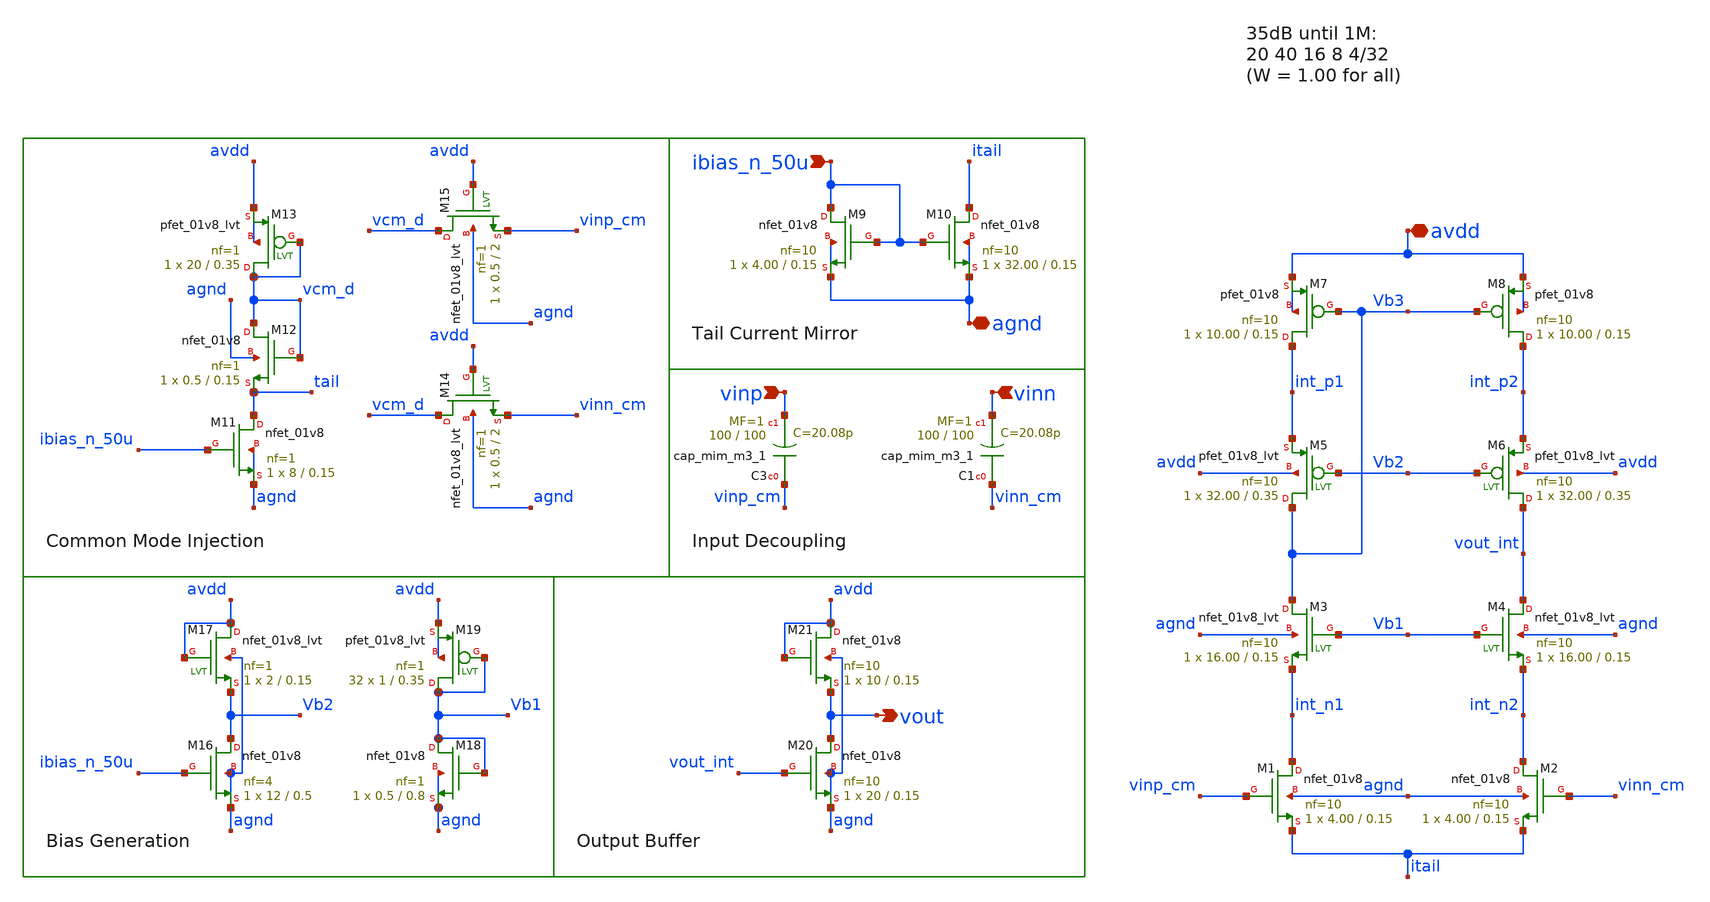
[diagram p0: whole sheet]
** sch_path: AMP/Final_Cascode_Mixed.sch
**.subckt Final_Cascode_Mixed avdd vinp vout agnd vinn ibias_n_50u
*.iopin avdd
*.ipin vinp
*.opin vout
*.iopin agnd
*.ipin vinn
*.ipin ibias_n_50u
XM1 int_n1 vinp_cm itail agnd sky130_fd_pr__nfet_01v8 L=0.15 W=4.00 nf=10 ad='int((nf+1)/2) * W/nf * 0.29'
+ as='int((nf+2)/2) * W/nf * 0.29' pd='2*int((nf+1)/2) * (W/nf + 0.29)' ps='2*int((nf+2)/2) * (W/nf + 0.29)'
+ nrd='0.29 / W' nrs='0.29 / W' sa=0 sb=0 sd=0 mult=1 m=1
XM2 int_n2 vinn_cm itail agnd sky130_fd_pr__nfet_01v8 L=0.15 W=4.00 nf=10 ad='int((nf+1)/2) * W/nf * 0.29'
+ as='int((nf+2)/2) * W/nf * 0.29' pd='2*int((nf+1)/2) * (W/nf + 0.29)' ps='2*int((nf+2)/2) * (W/nf + 0.29)'
+ nrd='0.29 / W' nrs='0.29 / W' sa=0 sb=0 sd=0 mult=1 m=1
XM7 int_p1 Vb3 avdd avdd sky130_fd_pr__pfet_01v8 L=0.15 W=10.00 nf=10 ad='int((nf+1)/2) * W/nf * 0.29'
+ as='int((nf+2)/2) * W/nf * 0.29' pd='2*int((nf+1)/2) * (W/nf + 0.29)' ps='2*int((nf+2)/2) * (W/nf + 0.29)'
+ nrd='0.29 / W' nrs='0.29 / W' sa=0 sb=0 sd=0 mult=1 m=1
XM8 int_p2 Vb3 avdd avdd sky130_fd_pr__pfet_01v8 L=0.15 W=10.00 nf=10 ad='int((nf+1)/2) * W/nf * 0.29'
+ as='int((nf+2)/2) * W/nf * 0.29' pd='2*int((nf+1)/2) * (W/nf + 0.29)' ps='2*int((nf+2)/2) * (W/nf + 0.29)'
+ nrd='0.29 / W' nrs='0.29 / W' sa=0 sb=0 sd=0 mult=1 m=1
XM9 ibias_n_50u ibias_n_50u agnd agnd sky130_fd_pr__nfet_01v8 L=0.15 W=4.00 nf=10 ad='int((nf+1)/2) * W/nf * 0.29'
+ as='int((nf+2)/2) * W/nf * 0.29' pd='2*int((nf+1)/2) * (W/nf + 0.29)' ps='2*int((nf+2)/2) * (W/nf + 0.29)'
+ nrd='0.29 / W' nrs='0.29 / W' sa=0 sb=0 sd=0 mult=1 m=1
XM10 itail ibias_n_50u agnd agnd sky130_fd_pr__nfet_01v8 L=0.15 W=32.00 nf=10 ad='int((nf+1)/2) * W/nf * 0.29'
+ as='int((nf+2)/2) * W/nf * 0.29' pd='2*int((nf+1)/2) * (W/nf + 0.29)' ps='2*int((nf+2)/2) * (W/nf + 0.29)'
+ nrd='0.29 / W' nrs='0.29 / W' sa=0 sb=0 sd=0 mult=1 m=1
XM3 Vb3 Vb1 int_n1 agnd sky130_fd_pr__nfet_01v8_lvt L=0.15 W=16.00 nf=10 ad='int((nf+1)/2) * W/nf * 0.29'
+ as='int((nf+2)/2) * W/nf * 0.29' pd='2*int((nf+1)/2) * (W/nf + 0.29)' ps='2*int((nf+2)/2) * (W/nf + 0.29)'
+ nrd='0.29 / W' nrs='0.29 / W' sa=0 sb=0 sd=0 mult=1 m=1
XM4 vout_int Vb1 int_n2 agnd sky130_fd_pr__nfet_01v8_lvt L=0.15 W=16.00 nf=10 ad='int((nf+1)/2) * W/nf * 0.29'
+ as='int((nf+2)/2) * W/nf * 0.29' pd='2*int((nf+1)/2) * (W/nf + 0.29)' ps='2*int((nf+2)/2) * (W/nf + 0.29)'
+ nrd='0.29 / W' nrs='0.29 / W' sa=0 sb=0 sd=0 mult=1 m=1
XM5 Vb3 Vb2 int_p1 avdd sky130_fd_pr__pfet_01v8_lvt L=0.35 W=32.00 nf=10 ad='int((nf+1)/2) * W/nf * 0.29'
+ as='int((nf+2)/2) * W/nf * 0.29' pd='2*int((nf+1)/2) * (W/nf + 0.29)' ps='2*int((nf+2)/2) * (W/nf + 0.29)'
+ nrd='0.29 / W' nrs='0.29 / W' sa=0 sb=0 sd=0 mult=1 m=1
XM6 vout_int Vb2 int_p2 avdd sky130_fd_pr__pfet_01v8_lvt L=0.35 W=32.00 nf=10 ad='int((nf+1)/2) * W/nf * 0.29'
+ as='int((nf+2)/2) * W/nf * 0.29' pd='2*int((nf+1)/2) * (W/nf + 0.29)' ps='2*int((nf+2)/2) * (W/nf + 0.29)'
+ nrd='0.29 / W' nrs='0.29 / W' sa=0 sb=0 sd=0 mult=1 m=1
XM11 tail ibias_n_50u agnd agnd sky130_fd_pr__nfet_01v8 L=0.15 W=8 nf=1 ad='int((nf+1)/2) * W/nf * 0.29'
+ as='int((nf+2)/2) * W/nf * 0.29' pd='2*int((nf+1)/2) * (W/nf + 0.29)' ps='2*int((nf+2)/2) * (W/nf + 0.29)'
+ nrd='0.29 / W' nrs='0.29 / W' sa=0 sb=0 sd=0 mult=1 m=1
XM12 vcm_d vcm_d tail agnd sky130_fd_pr__nfet_01v8 L=0.15 W=0.5 nf=1 ad='int((nf+1)/2) * W/nf * 0.29'
+ as='int((nf+2)/2) * W/nf * 0.29' pd='2*int((nf+1)/2) * (W/nf + 0.29)' ps='2*int((nf+2)/2) * (W/nf + 0.29)'
+ nrd='0.29 / W' nrs='0.29 / W' sa=0 sb=0 sd=0 mult=1 m=1
XM13 vcm_d vcm_d avdd avdd sky130_fd_pr__pfet_01v8_lvt L=0.35 W=20 nf=1 ad='int((nf+1)/2) * W/nf * 0.29'
+ as='int((nf+2)/2) * W/nf * 0.29' pd='2*int((nf+1)/2) * (W/nf + 0.29)' ps='2*int((nf+2)/2) * (W/nf + 0.29)'
+ nrd='0.29 / W' nrs='0.29 / W' sa=0 sb=0 sd=0 mult=1 m=1
XM14 vcm_d avdd vinn_cm agnd sky130_fd_pr__nfet_01v8_lvt L=2 W=0.5 nf=1 ad='int((nf+1)/2) * W/nf * 0.29'
+ as='int((nf+2)/2) * W/nf * 0.29' pd='2*int((nf+1)/2) * (W/nf + 0.29)' ps='2*int((nf+2)/2) * (W/nf + 0.29)'
+ nrd='0.29 / W' nrs='0.29 / W' sa=0 sb=0 sd=0 mult=1 m=1
XM15 vcm_d avdd vinp_cm agnd sky130_fd_pr__nfet_01v8_lvt L=2 W=0.5 nf=1 ad='int((nf+1)/2) * W/nf * 0.29'
+ as='int((nf+2)/2) * W/nf * 0.29' pd='2*int((nf+1)/2) * (W/nf + 0.29)' ps='2*int((nf+2)/2) * (W/nf + 0.29)'
+ nrd='0.29 / W' nrs='0.29 / W' sa=0 sb=0 sd=0 mult=1 m=1
XC3 vinp_cm vinp sky130_fd_pr__cap_mim_m3_1 W=100 L=100 MF=1 m=1
XC1 vinn_cm vinn sky130_fd_pr__cap_mim_m3_1 W=100 L=100 MF=1 m=1
XM16 Vb2 ibias_n_50u agnd agnd sky130_fd_pr__nfet_01v8 L=0.5 W=12 nf=4 ad='int((nf+1)/2) * W/nf * 0.29'
+ as='int((nf+2)/2) * W/nf * 0.29' pd='2*int((nf+1)/2) * (W/nf + 0.29)' ps='2*int((nf+2)/2) * (W/nf + 0.29)'
+ nrd='0.29 / W' nrs='0.29 / W' sa=0 sb=0 sd=0 mult=1 m=1
XM17 avdd avdd Vb2 agnd sky130_fd_pr__nfet_01v8_lvt L=0.15 W=2 nf=1 ad='int((nf+1)/2) * W/nf * 0.29'
+ as='int((nf+2)/2) * W/nf * 0.29' pd='2*int((nf+1)/2) * (W/nf + 0.29)' ps='2*int((nf+2)/2) * (W/nf + 0.29)'
+ nrd='0.29 / W' nrs='0.29 / W' sa=0 sb=0 sd=0 mult=1 m=1
XM19 Vb1 Vb1 avdd avdd sky130_fd_pr__pfet_01v8_lvt L=0.35 W=1 nf=1 ad='int((nf+1)/2) * W/nf * 0.29' as='int((nf+2)/2) * W/nf * 0.29'
+ pd='2*int((nf+1)/2) * (W/nf + 0.29)' ps='2*int((nf+2)/2) * (W/nf + 0.29)' nrd='0.29 / W' nrs='0.29 / W'
+ sa=0 sb=0 sd=0 mult=32 m=32
XM18 Vb1 Vb1 agnd agnd sky130_fd_pr__nfet_01v8 L=0.8 W=0.5 nf=1 ad='int((nf+1)/2) * W/nf * 0.29' as='int((nf+2)/2) * W/nf * 0.29'
+ pd='2*int((nf+1)/2) * (W/nf + 0.29)' ps='2*int((nf+2)/2) * (W/nf + 0.29)' nrd='0.29 / W' nrs='0.29 / W'
+ sa=0 sb=0 sd=0 mult=1 m=1
XM20 vout vout_int agnd agnd sky130_fd_pr__nfet_01v8 L=0.15 W=20 nf=10 ad='int((nf+1)/2) * W/nf * 0.29'
+ as='int((nf+2)/2) * W/nf * 0.29' pd='2*int((nf+1)/2) * (W/nf + 0.29)' ps='2*int((nf+2)/2) * (W/nf + 0.29)'
+ nrd='0.29 / W' nrs='0.29 / W' sa=0 sb=0 sd=0 mult=1 m=1
XM21 avdd avdd vout agnd sky130_fd_pr__nfet_01v8 L=0.15 W=10 nf=10 ad='int((nf+1)/2) * W/nf * 0.29' as='int((nf+2)/2) * W/nf * 0.29'
+ pd='2*int((nf+1)/2) * (W/nf + 0.29)' ps='2*int((nf+2)/2) * (W/nf + 0.29)' nrd='0.29 / W' nrs='0.29 / W'
+ sa=0 sb=0 sd=0 mult=1 m=1
**.ends
.end
